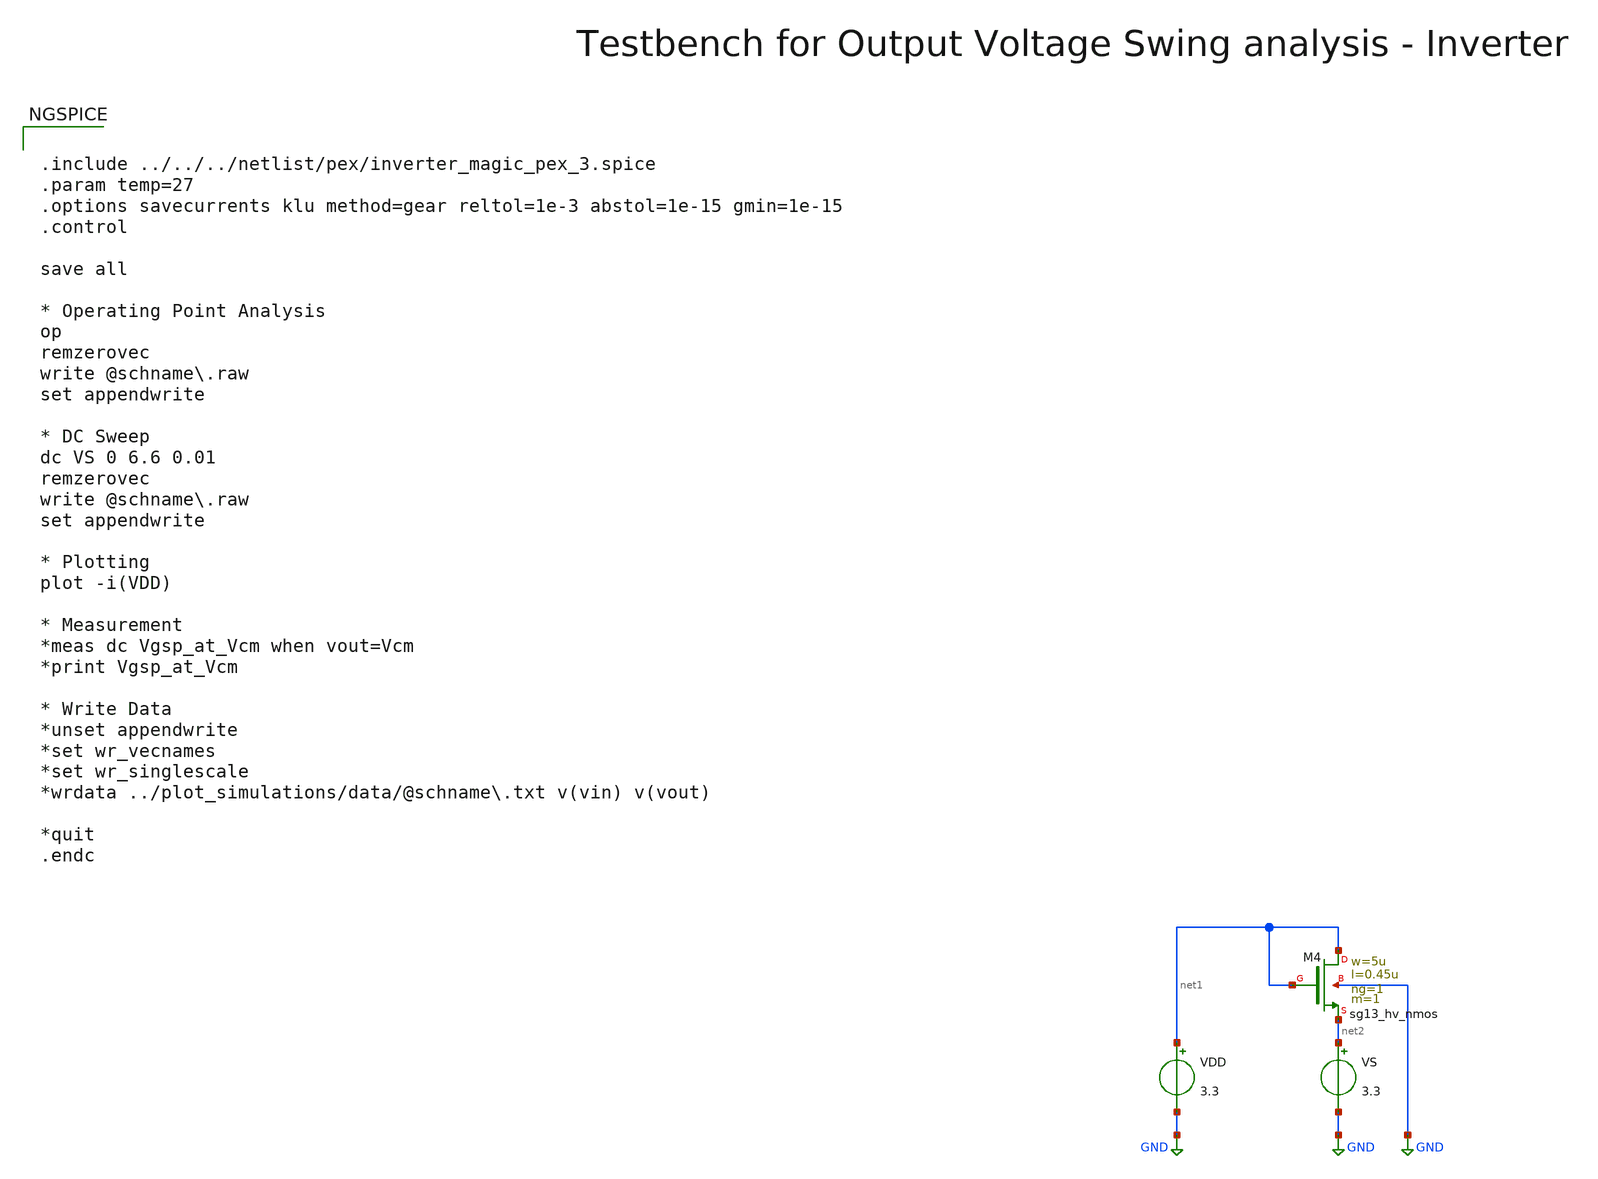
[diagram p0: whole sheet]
** sch_path: macros/heichips26_vcr/macros/switched_capacitor/testbenches/xschem/tb_nmos_diode_dc.sch
**.subckt tb_nmos_diode_dc
VDD net1 GND 3.3
XM4 net1 net1 net2 GND sg13_hv_nmos w=5u l=0.45u ng=1 m=1 mm_ok=1
VS net2 GND 3.3
**** begin user architecture code


.include ../../../netlist/pex/inverter_magic_pex_3.spice
.param temp=27
.options savecurrents klu method=gear reltol=1e-3 abstol=1e-15 gmin=1e-15
.control

save all

* Operating Point Analysis
op
remzerovec
write @schname\.raw
set appendwrite

* DC Sweep
dc VS 0 6.6 0.01
remzerovec
write @schname\.raw
set appendwrite

* Plotting
plot -i(VDD)

* Measurement
*meas dc Vgsp_at_Vcm when vout=Vcm
*print Vgsp_at_Vcm

* Write Data
*unset appendwrite
*set wr_vecnames
*set wr_singlescale
*wrdata ../plot_simulations/data/@schname\.txt v(vin) v(vout)

*quit
.endc



.lib cornerMOSlv.lib mos_tt
.lib cornerMOShv.lib mos_tt
.lib cornerRES.lib res_typ
.lib cornerDIO.lib dio_tt

**** end user architecture code
**.ends
.GLOBAL GND
.end
